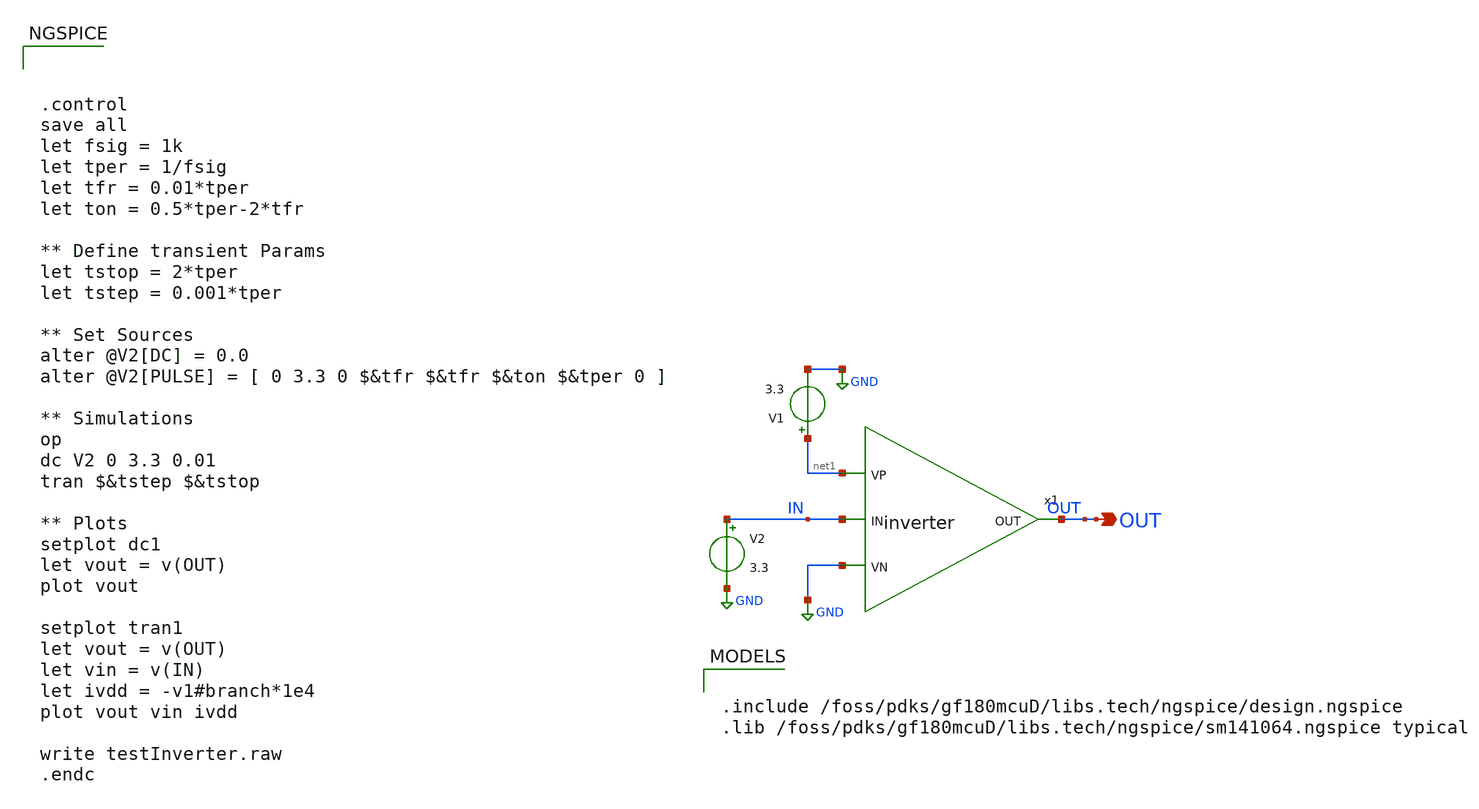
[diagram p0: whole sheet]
** sch_path: designs/libs/Inverter/testInverter.sch
**.subckt testInverter OUT
*.opin OUT
x1 IN OUT net1 GND inverter
V1 net1 GND 3.3
V2 IN GND 3.3
**** begin user architecture code



.control
save all
let fsig = 1k
let tper = 1/fsig
let tfr = 0.01*tper
let ton = 0.5*tper-2*tfr

** Define transient Params
let tstop = 2*tper
let tstep = 0.001*tper

** Set Sources
alter @V2[DC] = 0.0
alter @V2[PULSE] = [ 0 3.3 0 $&tfr $&tfr $&ton $&tper 0 ]

** Simulations
op
dc V2 0 3.3 0.01
tran $&tstep $&tstop

** Plots
setplot dc1
let vout = v(OUT)
plot vout

setplot tran1
let vout = v(OUT)
let vin = v(IN)
let ivdd = -v1#branch*1e4
plot vout vin ivdd

write testInverter.raw
.endc



.include /foss/pdks/gf180mcuD/libs.tech/ngspice/design.ngspice
.lib /foss/pdks/gf180mcuD/libs.tech/ngspice/sm141064.ngspice typical

**** end user architecture code
**.ends

* expanding   symbol:  gf180mcuD/test/inverter.sym # of pins=4
** sym_path: designs/libs/Inverter/inverter.sym
** sch_path: designs/libs/Inverter/inverter.sch
.subckt inverter IN OUT VP VN
*.ipin IN
*.opin OUT
*.ipin VP
*.ipin VN
XM1 OUT IN VN VN nfet_03v3 L=0.28u W=0.22u nf=1 ad='int((nf+1)/2) * W/nf * 0.18u' as='int((nf+2)/2) * W/nf * 0.18u'
+ pd='2*int((nf+1)/2) * (W/nf + 0.18u)' ps='2*int((nf+2)/2) * (W/nf + 0.18u)' nrd='0.18u / W' nrs='0.18u / W'
+ sa=0 sb=0 sd=0 m=1
XM2 OUT IN VP VP pfet_03v3 L=0.28u W=0.22u nf=1 ad='int((nf+1)/2) * W/nf * 0.18u' as='int((nf+2)/2) * W/nf * 0.18u'
+ pd='2*int((nf+1)/2) * (W/nf + 0.18u)' ps='2*int((nf+2)/2) * (W/nf + 0.18u)' nrd='0.18u / W' nrs='0.18u / W'
+ sa=0 sb=0 sd=0 m=1
.ends

.GLOBAL GND
.end
